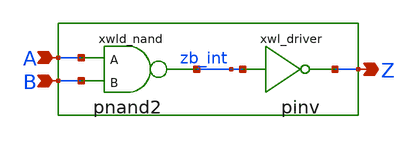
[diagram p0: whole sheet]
** sch_path: sram_4_16_scn4m/wordline_driver.sch
**.subckt wordline_driver A B Z
*.ipin A
*.ipin B
*.opin Z
xwld_nand A B zb_int vdd gnd pnand2
xwl_driver zb_int Z vdd gnd pinv
**.ends

* expanding   symbol:  pnand2.sym # of pins=3
** sym_path: sram_2_64_scn4m/pnand2.sym
** sch_path: sram_2_64_scn4m/pnand2.sch
.subckt pnand2 A B Z vdd gnd
*.ipin A
*.ipin B
*.opin Z
*.iopin vdd
*.iopin gnd
XMpnand2_nmos1 Z B net1 gnd sky130_fd_pr__nfet_01v8 L=0.4 W=1.6 nf=1 ad='int((nf+1)/2) * W/nf * 0.29'
+ as='int((nf+2)/2) * W/nf * 0.29' pd='2*int((nf+1)/2) * (W/nf + 0.29)' ps='2*int((nf+2)/2) * (W/nf + 0.29)'
+ nrd='0.29 / W' nrs='0.29 / W' sa=0 sb=0 sd=0 mult=1 m=1
XMpnand2_pmos1 Z A vdd vdd sky130_fd_pr__pfet_01v8 L=0.4 W=1.6 nf=1 ad='int((nf+1)/2) * W/nf * 0.29'
+ as='int((nf+2)/2) * W/nf * 0.29' pd='2*int((nf+1)/2) * (W/nf + 0.29)' ps='2*int((nf+2)/2) * (W/nf + 0.29)'
+ nrd='0.29 / W' nrs='0.29 / W' sa=0 sb=0 sd=0 mult=1 m=1
XMpnand2_pmos2 Z B vdd vdd sky130_fd_pr__pfet_01v8 L=0.4 W=1.6 nf=1 ad='int((nf+1)/2) * W/nf * 0.29'
+ as='int((nf+2)/2) * W/nf * 0.29' pd='2*int((nf+1)/2) * (W/nf + 0.29)' ps='2*int((nf+2)/2) * (W/nf + 0.29)'
+ nrd='0.29 / W' nrs='0.29 / W' sa=0 sb=0 sd=0 mult=1 m=1
XMpnand2_nmos2 net1 A gnd gnd sky130_fd_pr__nfet_01v8 L=0.4 W=1.6 nf=1 ad='int((nf+1)/2) * W/nf * 0.29'
+ as='int((nf+2)/2) * W/nf * 0.29' pd='2*int((nf+1)/2) * (W/nf + 0.29)' ps='2*int((nf+2)/2) * (W/nf + 0.29)'
+ nrd='0.29 / W' nrs='0.29 / W' sa=0 sb=0 sd=0 mult=1 m=1
.ends


* expanding   symbol:  pinv.sym # of pins=2
** sym_path: sram_4_16_scn4m/pinv.sym
** sch_path: sram_4_16_scn4m/pinv.sch
.subckt pinv A Z vdd gnd
*.ipin A
*.opin Z
XMpinv_nmos Z A gnd gnd sky130_fd_pr__nfet_01v8 L=0.4 W=0.8 nf=1 ad='int((nf+1)/2) * W/nf * 0.29' as='int((nf+2)/2) * W/nf * 0.29'
+ pd='2*int((nf+1)/2) * (W/nf + 0.29)' ps='2*int((nf+2)/2) * (W/nf + 0.29)' nrd='0.29 / W' nrs='0.29 / W'
+ sa=0 sb=0 sd=0 mult=1 m=1
XMp_inv_pmos Z A vdd vdd sky130_fd_pr__pfet_01v8 L=0.4 W=1.6 nf=1 ad='int((nf+1)/2) * W/nf * 0.29' as='int((nf+2)/2) * W/nf * 0.29'
+ pd='2*int((nf+1)/2) * (W/nf + 0.29)' ps='2*int((nf+2)/2) * (W/nf + 0.29)' nrd='0.29 / W' nrs='0.29 / W'
+ sa=0 sb=0 sd=0 mult=1 m=1
.ends

.end
